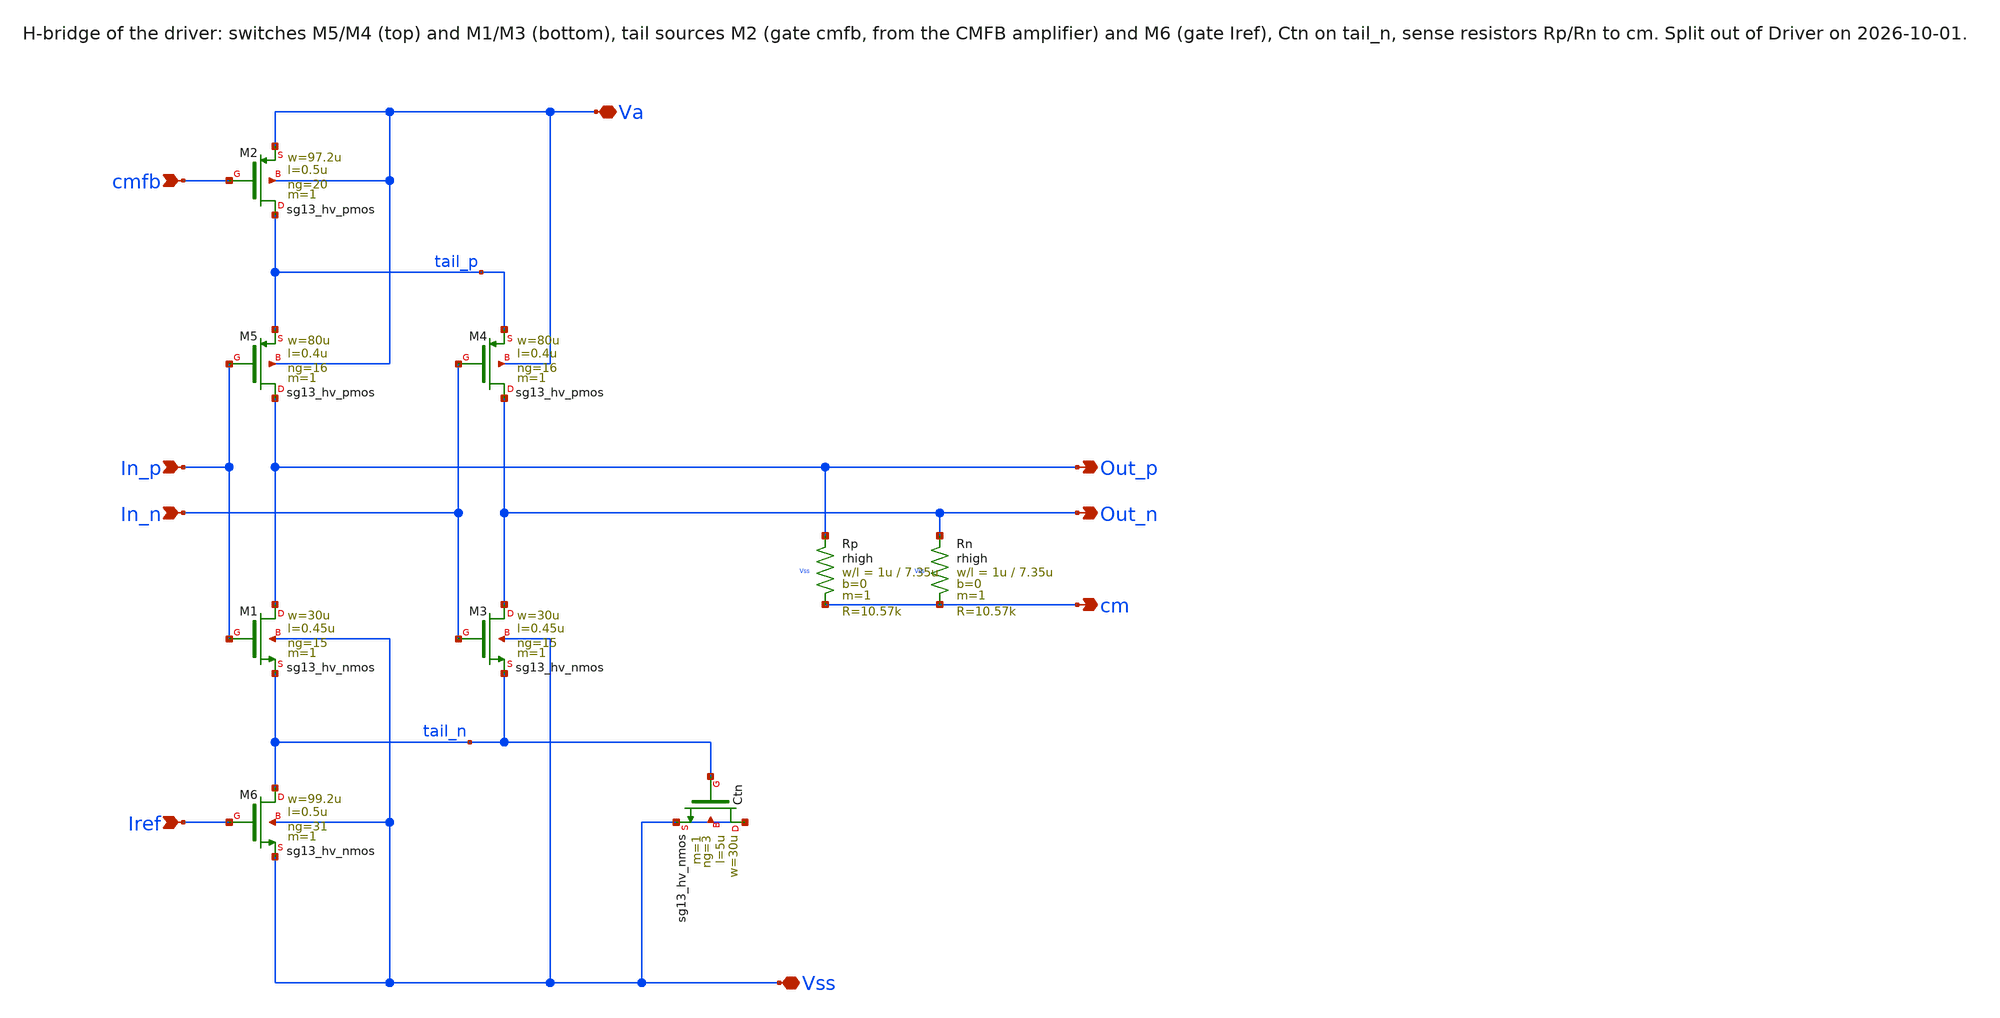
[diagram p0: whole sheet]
** sch_path: macros/lvds_tx/schematic/xschem/hbridge.sch
**.subckt hbridge Va Vss In_p In_n Iref cmfb Out_p Out_n cm
*.iopin Va
*.iopin Vss
*.ipin In_p
*.ipin In_n
*.ipin Iref
*.ipin cmfb
*.opin Out_p
*.opin Out_n
*.opin cm
XCtn Vss tail_n Vss Vss sg13_hv_nmos w=30u l=5u ng=3 m=1 mm_ok=1
XM2 tail_p cmfb Va Va sg13_hv_pmos w=97.2u l=0.5u ng=20 m=1 mm_ok=1
XM5 Out_p In_p tail_p Va sg13_hv_pmos w=80u l=0.4u ng=16 m=1 mm_ok=1
XM4 Out_n In_n tail_p Va sg13_hv_pmos w=80u l=0.4u ng=16 m=1 mm_ok=1
XM1 Out_p In_p tail_n Vss sg13_hv_nmos w=30u l=0.45u ng=15 m=1 mm_ok=1
XM3 Out_n In_n tail_n Vss sg13_hv_nmos w=30u l=0.45u ng=15 m=1 mm_ok=1
XM6 tail_n Iref Vss Vss sg13_hv_nmos w=99.2u l=0.5u ng=31 m=1 mm_ok=1
XRp Out_p cm Vss rhigh w=1u l=7.35u m=1 b=0 mm_ok=1
XRn Out_n cm Vss rhigh w=1u l=7.35u m=1 b=0 mm_ok=1
**.ends
.end
